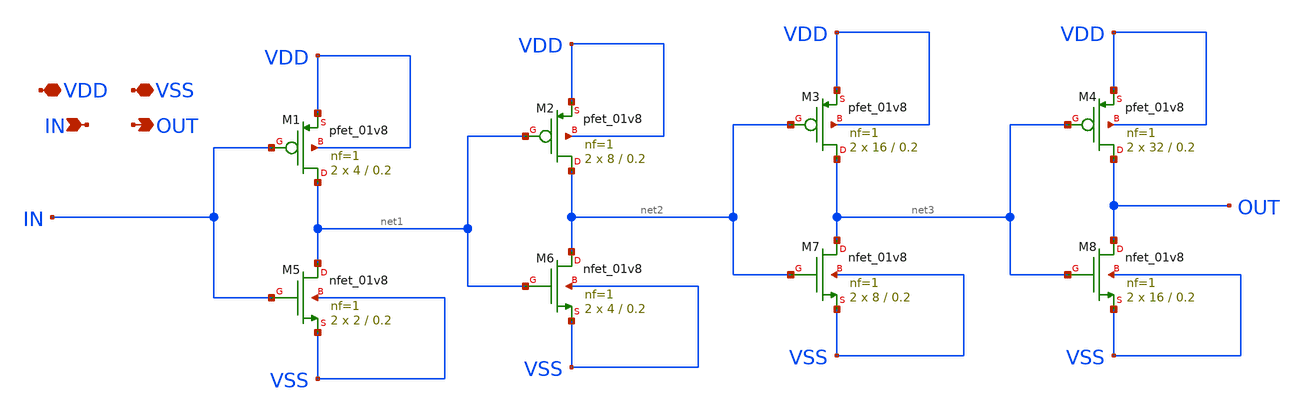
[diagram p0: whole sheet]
** sch_path: Xschem/PLL_TOP_Schematics/Tappered-Buffer_1.sch
**.subckt Tappered-Buffer_1 VDD VSS IN OUT
*.iopin VDD
*.iopin VSS
*.ipin IN
*.opin OUT
XM1 net1 IN VDD VDD sky130_fd_pr__pfet_01v8 L=0.2 W=4 nf=1 ad='int((nf+1)/2) * W/nf * 0.29' as='int((nf+2)/2) * W/nf * 0.29'
+ pd='2*int((nf+1)/2) * (W/nf + 0.29)' ps='2*int((nf+2)/2) * (W/nf + 0.29)' nrd='0.29 / W' nrs='0.29 / W'
+ sa=0 sb=0 sd=0 mult=2 m=2
XM2 net2 net1 VDD VDD sky130_fd_pr__pfet_01v8 L=0.2 W=8 nf=1 ad='int((nf+1)/2) * W/nf * 0.29' as='int((nf+2)/2) * W/nf * 0.29'
+ pd='2*int((nf+1)/2) * (W/nf + 0.29)' ps='2*int((nf+2)/2) * (W/nf + 0.29)' nrd='0.29 / W' nrs='0.29 / W'
+ sa=0 sb=0 sd=0 mult=2 m=2
XM3 net3 net2 VDD VDD sky130_fd_pr__pfet_01v8 L=0.2 W=16 nf=1 ad='int((nf+1)/2) * W/nf * 0.29' as='int((nf+2)/2) * W/nf * 0.29'
+ pd='2*int((nf+1)/2) * (W/nf + 0.29)' ps='2*int((nf+2)/2) * (W/nf + 0.29)' nrd='0.29 / W' nrs='0.29 / W'
+ sa=0 sb=0 sd=0 mult=2 m=2
XM5 net1 IN VSS VSS sky130_fd_pr__nfet_01v8 L=0.2 W=2 nf=1 ad='int((nf+1)/2) * W/nf * 0.29' as='int((nf+2)/2) * W/nf * 0.29'
+ pd='2*int((nf+1)/2) * (W/nf + 0.29)' ps='2*int((nf+2)/2) * (W/nf + 0.29)' nrd='0.29 / W' nrs='0.29 / W'
+ sa=0 sb=0 sd=0 mult=2 m=2
XM6 net2 net1 VSS VSS sky130_fd_pr__nfet_01v8 L=0.2 W=4 nf=1 ad='int((nf+1)/2) * W/nf * 0.29' as='int((nf+2)/2) * W/nf * 0.29'
+ pd='2*int((nf+1)/2) * (W/nf + 0.29)' ps='2*int((nf+2)/2) * (W/nf + 0.29)' nrd='0.29 / W' nrs='0.29 / W'
+ sa=0 sb=0 sd=0 mult=2 m=2
XM7 net3 net2 VSS VSS sky130_fd_pr__nfet_01v8 L=0.2 W=8 nf=1 ad='int((nf+1)/2) * W/nf * 0.29' as='int((nf+2)/2) * W/nf * 0.29'
+ pd='2*int((nf+1)/2) * (W/nf + 0.29)' ps='2*int((nf+2)/2) * (W/nf + 0.29)' nrd='0.29 / W' nrs='0.29 / W'
+ sa=0 sb=0 sd=0 mult=2 m=2
XM4 OUT net3 VDD VDD sky130_fd_pr__pfet_01v8 L=0.2 W=32 nf=1 ad='int((nf+1)/2) * W/nf * 0.29' as='int((nf+2)/2) * W/nf * 0.29'
+ pd='2*int((nf+1)/2) * (W/nf + 0.29)' ps='2*int((nf+2)/2) * (W/nf + 0.29)' nrd='0.29 / W' nrs='0.29 / W'
+ sa=0 sb=0 sd=0 mult=2 m=2
XM8 OUT net3 VSS VSS sky130_fd_pr__nfet_01v8 L=0.2 W=16 nf=1 ad='int((nf+1)/2) * W/nf * 0.29' as='int((nf+2)/2) * W/nf * 0.29'
+ pd='2*int((nf+1)/2) * (W/nf + 0.29)' ps='2*int((nf+2)/2) * (W/nf + 0.29)' nrd='0.29 / W' nrs='0.29 / W'
+ sa=0 sb=0 sd=0 mult=2 m=2
**.ends
.end
